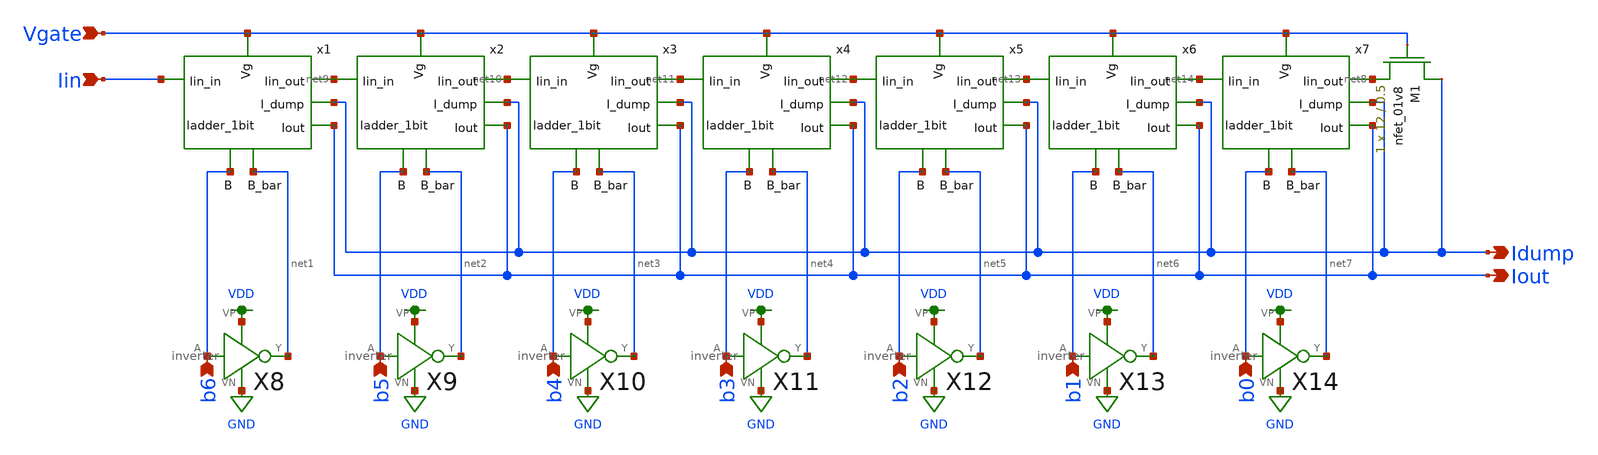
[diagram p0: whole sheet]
** sch_path: ladder_7bit.sch
**.subckt ladder_7bit Idump Iout Vgate Iin b6 b5 b4 b3 b2 b1 b0
*.opin Idump
*.opin Iout
*.ipin Vgate
*.ipin Iin
*.ipin b6
*.ipin b5
*.ipin b4
*.ipin b3
*.ipin b2
*.ipin b1
*.ipin b0
XM1 Idump Vgate net8 GND sky130_fd_pr__nfet_01v8 L=0.5 W=12 nf=1 ad='int((nf+1)/2) * W/nf * 0.29' as='int((nf+2)/2) * W/nf * 0.29'
+ pd='2*int((nf+1)/2) * (W/nf + 0.29)' ps='2*int((nf+2)/2) * (W/nf + 0.29)' nrd='0.29 / W' nrs='0.29 / W'
+ sa=0 sb=0 sd=0 mult=1 m=1
x1 Iin net9 Vgate Idump Iout net1 b6 ladder_1bit
X8 b6 net1 VDD GND inverter
X9 b5 net2 VDD GND inverter
X10 b4 net3 VDD GND inverter
X11 b3 net4 VDD GND inverter
X12 b2 net5 VDD GND inverter
X13 b1 net6 VDD GND inverter
X14 b0 net7 VDD GND inverter
x2 net9 net10 Vgate Idump Iout net2 b5 ladder_1bit
x3 net10 net11 Vgate Idump Iout net3 b4 ladder_1bit
x4 net11 net12 Vgate Idump Iout net4 b3 ladder_1bit
x5 net12 net13 Vgate Idump Iout net5 b2 ladder_1bit
x6 net13 net14 Vgate Idump Iout net6 b1 ladder_1bit
x7 net14 net8 Vgate Idump Iout net7 b0 ladder_1bit
**.ends
.GLOBAL VDD
.GLOBAL GND
.end
